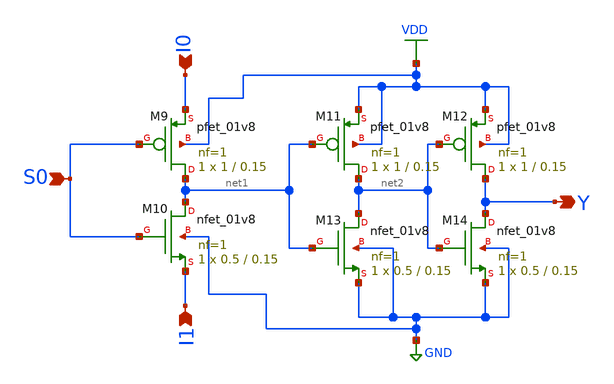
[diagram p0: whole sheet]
** sch_path: xschem/mux2.sch
**.subckt mux2 I1 I0 S0 Y
*.ipin I1
*.ipin I0
*.ipin S0
*.opin Y
XM9 net1 S0 I0 VDD sky130_fd_pr__pfet_01v8 L=0.15 W=1 nf=1 ad='int((nf+1)/2) * W/nf * 0.29' as='int((nf+2)/2) * W/nf * 0.29'
+ pd='2*int((nf+1)/2) * (W/nf + 0.29)' ps='2*int((nf+2)/2) * (W/nf + 0.29)' nrd='0.29 / W' nrs='0.29 / W'
+ sa=0 sb=0 sd=0 mult=1 m=1
XM10 net1 S0 I1 GND sky130_fd_pr__nfet_01v8 L=0.15 W=0.5 nf=1 ad='int((nf+1)/2) * W/nf * 0.29' as='int((nf+2)/2) * W/nf * 0.29'
+ pd='2*int((nf+1)/2) * (W/nf + 0.29)' ps='2*int((nf+2)/2) * (W/nf + 0.29)' nrd='0.29 / W' nrs='0.29 / W'
+ sa=0 sb=0 sd=0 mult=1 m=1
XM11 net2 net1 VDD VDD sky130_fd_pr__pfet_01v8 L=0.15 W=1 nf=1 ad='int((nf+1)/2) * W/nf * 0.29' as='int((nf+2)/2) * W/nf * 0.29'
+ pd='2*int((nf+1)/2) * (W/nf + 0.29)' ps='2*int((nf+2)/2) * (W/nf + 0.29)' nrd='0.29 / W' nrs='0.29 / W'
+ sa=0 sb=0 sd=0 mult=1 m=1
XM12 Y net2 VDD VDD sky130_fd_pr__pfet_01v8 L=0.15 W=1 nf=1 ad='int((nf+1)/2) * W/nf * 0.29' as='int((nf+2)/2) * W/nf * 0.29'
+ pd='2*int((nf+1)/2) * (W/nf + 0.29)' ps='2*int((nf+2)/2) * (W/nf + 0.29)' nrd='0.29 / W' nrs='0.29 / W'
+ sa=0 sb=0 sd=0 mult=1 m=1
XM13 net2 net1 GND GND sky130_fd_pr__nfet_01v8 L=0.15 W=0.5 nf=1 ad='int((nf+1)/2) * W/nf * 0.29' as='int((nf+2)/2) * W/nf * 0.29'
+ pd='2*int((nf+1)/2) * (W/nf + 0.29)' ps='2*int((nf+2)/2) * (W/nf + 0.29)' nrd='0.29 / W' nrs='0.29 / W'
+ sa=0 sb=0 sd=0 mult=1 m=1
XM14 Y net2 GND GND sky130_fd_pr__nfet_01v8 L=0.15 W=0.5 nf=1 ad='int((nf+1)/2) * W/nf * 0.29' as='int((nf+2)/2) * W/nf * 0.29'
+ pd='2*int((nf+1)/2) * (W/nf + 0.29)' ps='2*int((nf+2)/2) * (W/nf + 0.29)' nrd='0.29 / W' nrs='0.29 / W'
+ sa=0 sb=0 sd=0 mult=1 m=1
**.ends
.GLOBAL VDD
.GLOBAL GND
.end
